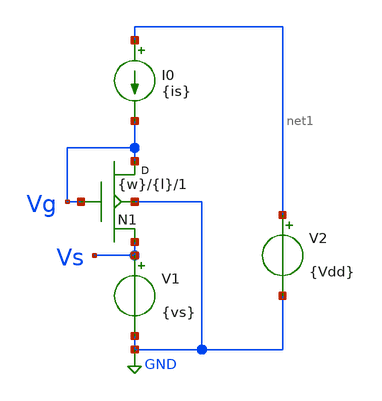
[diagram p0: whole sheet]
** sch_path: Parametros_Vaf/n_test.sch
**.subckt n_test
V1 Vs GND {vs}
V2 net1 GND {Vdd}
I0 net1 Vg {is}
N1 Vg Vg Vs GND NMOS_ACM w={w} l={l} m=1
**** begin user architecture code


* Circuit Parameters
.param vs = 3
.param step = 0.01
.param Vdd = 1.8
.param is = 0.173u
.param w = 5.0u
.param l = 0.18u
* Include Models
.model NMOS_ACM nmos_ACM
.model PMOS_ACM pmos_ACM
* OP Parameters & Singals to save
.save all
*Simulations
.dc V1 -1 {vs} {step}
.control
pre_osdi NMOS_ACM_2V0.osdi
pre_osdi PMOS_ACM_2V0.osdi
run
setplot dc1
plot v(Vg)
set filetype = ascii
write dcsweep.raw
.endc
.end


**** end user architecture code
**.ends
.GLOBAL GND
.end
